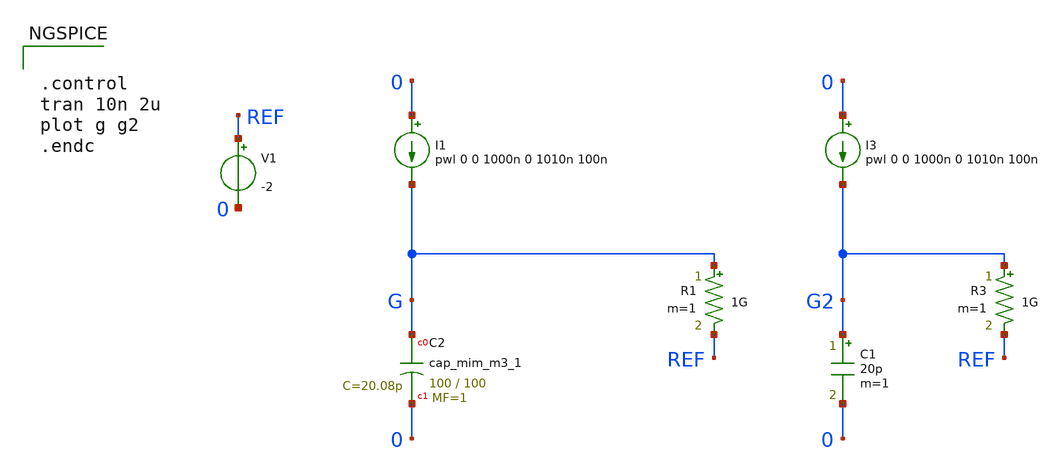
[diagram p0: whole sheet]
** sch_path: test_sky_cap.sch
* Copyright 2021 Stefan Frederik Schippers
* Licensed under the Apache License, Version 2.0 (the "License");
* you may not use this file except in compliance with the License.
* You may obtain a copy of the License at
* https://www.apache.org/licenses/LICENSE-2.0
* Unless required by applicable law or agreed to in writing, software
* distributed under the License is distributed on an "AS IS" BASIS,
* WITHOUT WARRANTIES OR CONDITIONS OF ANY KIND, either express or implied.
* See the License for the specific language governing permissions and
* limitations under the License.
**.subckt test_sky_cap
I1 0 G pwl 0 0 1000n 0 1010n 100n
R1 G REF 1G m=1
I3 0 G2 pwl 0 0 1000n 0 1010n 100n
R3 G2 REF 1G m=1
C1 G2 0 20p m=1
V1 REF 0 -2
XC2 G 0 sky130_fd_pr__cap_mim_m3_1 W=100 L=100 MF=1 m=1
**** begin user architecture code


.control
tran 10n 2u
plot g g2
.endc



** opencircuitdesign pdks install
.lib $::SKYWATER_MODELS/sky130.lib.spice tt


**** end user architecture code
**.ends
.end
